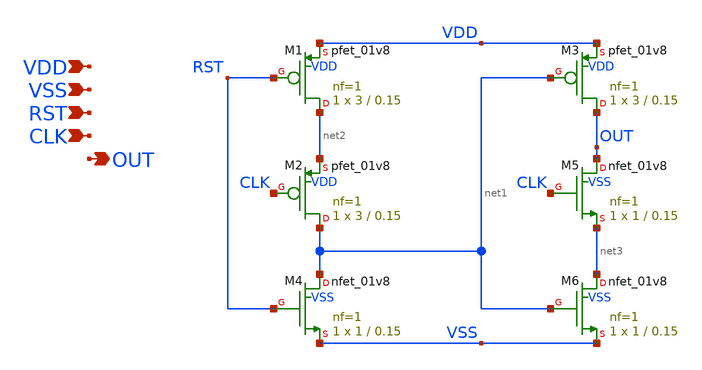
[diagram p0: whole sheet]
** sch_path: xschem/tscp.sch
**.subckt tscp VDD VSS RST CLK OUT
*.ipin VDD
*.ipin VSS
*.ipin RST
*.ipin CLK
*.opin OUT
XM1 net2 RST VDD VDD sky130_fd_pr__pfet_01v8 L=0.15 W=3 nf=1 ad='int((nf+1)/2) * W/nf * 0.29' as='int((nf+2)/2) * W/nf * 0.29'
+ pd='2*int((nf+1)/2) * (W/nf + 0.29)' ps='2*int((nf+2)/2) * (W/nf + 0.29)' nrd='0.29 / W' nrs='0.29 / W'
+ sa=0 sb=0 sd=0 mult=1 m=1
XM2 net1 CLK net2 VDD sky130_fd_pr__pfet_01v8 L=0.15 W=3 nf=1 ad='int((nf+1)/2) * W/nf * 0.29' as='int((nf+2)/2) * W/nf * 0.29'
+ pd='2*int((nf+1)/2) * (W/nf + 0.29)' ps='2*int((nf+2)/2) * (W/nf + 0.29)' nrd='0.29 / W' nrs='0.29 / W'
+ sa=0 sb=0 sd=0 mult=1 m=1
XM3 OUT net1 VDD VDD sky130_fd_pr__pfet_01v8 L=0.15 W=3 nf=1 ad='int((nf+1)/2) * W/nf * 0.29' as='int((nf+2)/2) * W/nf * 0.29'
+ pd='2*int((nf+1)/2) * (W/nf + 0.29)' ps='2*int((nf+2)/2) * (W/nf + 0.29)' nrd='0.29 / W' nrs='0.29 / W'
+ sa=0 sb=0 sd=0 mult=1 m=1
XM4 net1 RST VSS VSS sky130_fd_pr__nfet_01v8 L=0.15 W=1 nf=1 ad='int((nf+1)/2) * W/nf * 0.29' as='int((nf+2)/2) * W/nf * 0.29'
+ pd='2*int((nf+1)/2) * (W/nf + 0.29)' ps='2*int((nf+2)/2) * (W/nf + 0.29)' nrd='0.29 / W' nrs='0.29 / W'
+ sa=0 sb=0 sd=0 mult=1 m=1
XM5 OUT CLK net3 VSS sky130_fd_pr__nfet_01v8 L=0.15 W=1 nf=1 ad='int((nf+1)/2) * W/nf * 0.29' as='int((nf+2)/2) * W/nf * 0.29'
+ pd='2*int((nf+1)/2) * (W/nf + 0.29)' ps='2*int((nf+2)/2) * (W/nf + 0.29)' nrd='0.29 / W' nrs='0.29 / W'
+ sa=0 sb=0 sd=0 mult=1 m=1
XM6 net3 net1 VSS VSS sky130_fd_pr__nfet_01v8 L=0.15 W=1 nf=1 ad='int((nf+1)/2) * W/nf * 0.29' as='int((nf+2)/2) * W/nf * 0.29'
+ pd='2*int((nf+1)/2) * (W/nf + 0.29)' ps='2*int((nf+2)/2) * (W/nf + 0.29)' nrd='0.29 / W' nrs='0.29 / W'
+ sa=0 sb=0 sd=0 mult=1 m=1
**.ends
.end
